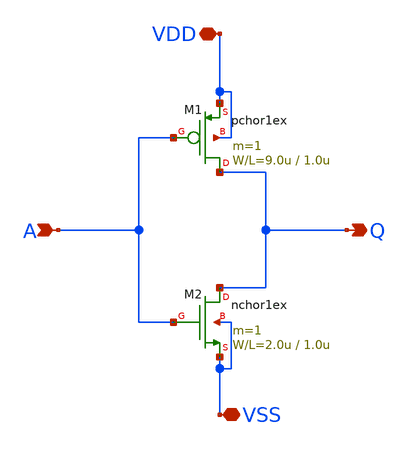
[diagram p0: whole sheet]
** sch_path: member_project/yato-Neco/inverter.sch
**.subckt inverter A Q VDD VSS
*.ipin A
*.opin Q
*.iopin VDD
*.iopin VSS
M1 Q A VDD VDD pchor1ex L=1.0u W=9.0u m=1
M2 Q A VSS VSS nchor1ex L=1.0u W=2.0u m=1
**.ends
.end
